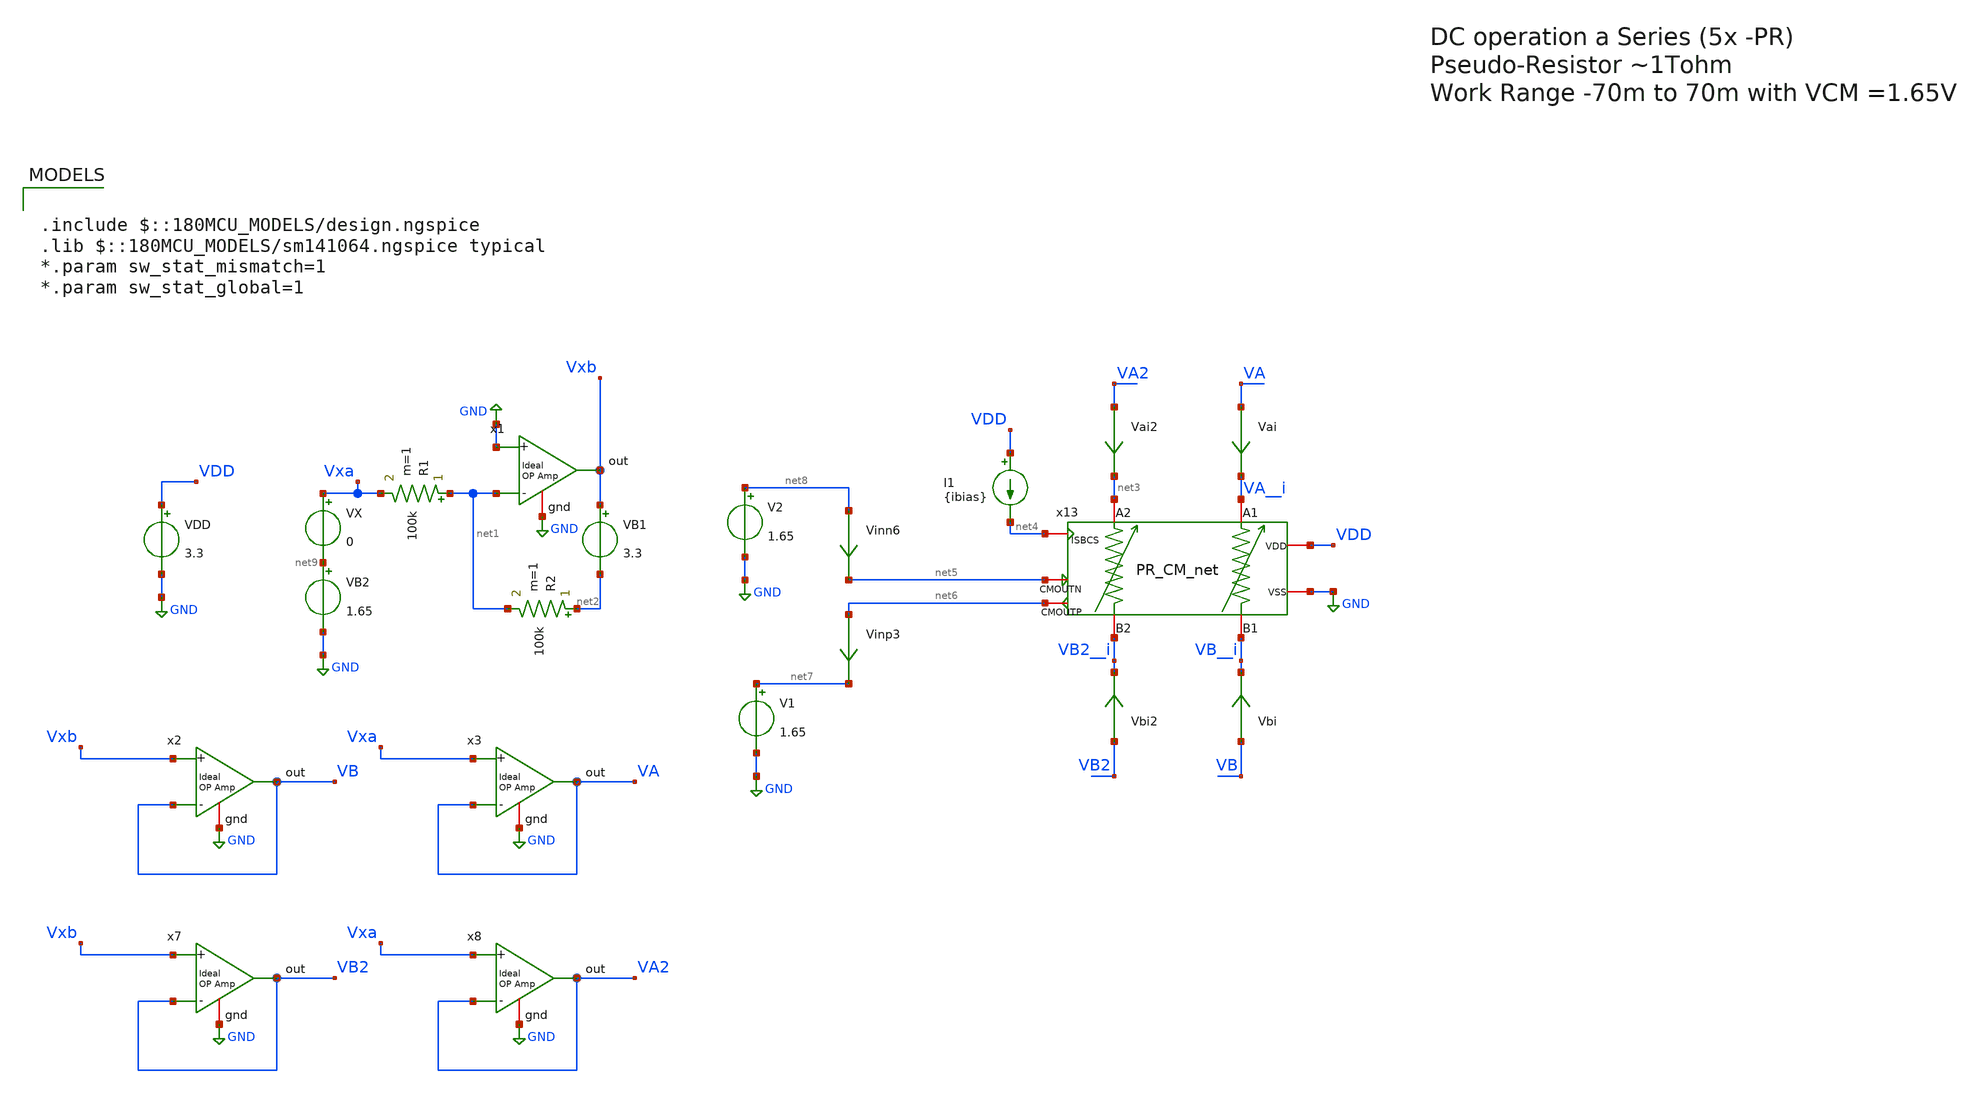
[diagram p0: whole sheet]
** sch_path: TIA_Filter/PseudoResistor/TB_PR_series_dc.sch
**.subckt TB_PR_series_dc
VDD VDD GND 3.3
VX Vxa net9 0
VB1 Vxb net2 3.3
R1 net1 Vxa 100k m=1
R2 net2 net1 100k m=1
VB2 net9 GND 1.65
x2 VB Vxb VB GND ampOp_ideal
x3 VA Vxa VA GND ampOp_ideal
x1 Vxb GND net1 GND ampOp_ideal
Vai VA VA__i 0
.save i(vai)
Vbi VB VB__i 0
.save i(vbi)
Vbi2 VB2 VB2__i 0
.save i(vbi2)
Vai2 VA2 net3 0
.save i(vai2)
x7 VB2 Vxb VB2 GND ampOp_ideal
x8 VA2 Vxa VA2 GND ampOp_ideal
x13 net4 VA__i net3 VB2__i VB__i net5 net6 VDD GND PR_CM_net
I1 VDD net4 {ibias}
Vinn6 net8 net5 0
.save i(vinn6)
Vinp3 net6 net7 0
.save i(vinp3)
V1 net7 GND 1.65
V2 net8 GND 1.65
**** begin user architecture code

.include $::180MCU_MODELS/design.ngspice
.lib $::180MCU_MODELS/sm141064.ngspice typical
*.param sw_stat_mismatch=1
*.param sw_stat_global=1



*.OPTION ABSTOL=1e-2
.option gmin=1e-15
*.option RSHUNT=1e35
.option klu

*.nodeset v(Vin_neg)=1.65
*.nodeset v(vout)=1.65

*.nodeset all=1.65

.param ibias = 1n
*.param it_amp = 2p

.control
save all

set temp = 27

op
remzerovec
write TB_PR_series_dc.raw
set appendwrite

dc VX -200m 200m 10m

let idiff = i(vai)-i(vbi)
let Rdiff = 4/deriv(idiff)

let idiff2 = i(vai2)-i(vbi2)
let Rdiff2 = 4/deriv(idiff2)

save idiff Rdiff idiff2 Rdiff2
remzerovec
write TB_PR_series_dc.raw
wrdata /home/gmaranhao/Desktop/Bracolin/TIA_Filter/PseudoResistor/plots/data_DC/PR_series_DC_m20.txt
+ idiff Rdiff idiff2 Rdiff2 V(x13.x11.x3.vc)

.endc


**** end user architecture code
**.ends
.GLOBAL GND
.end
